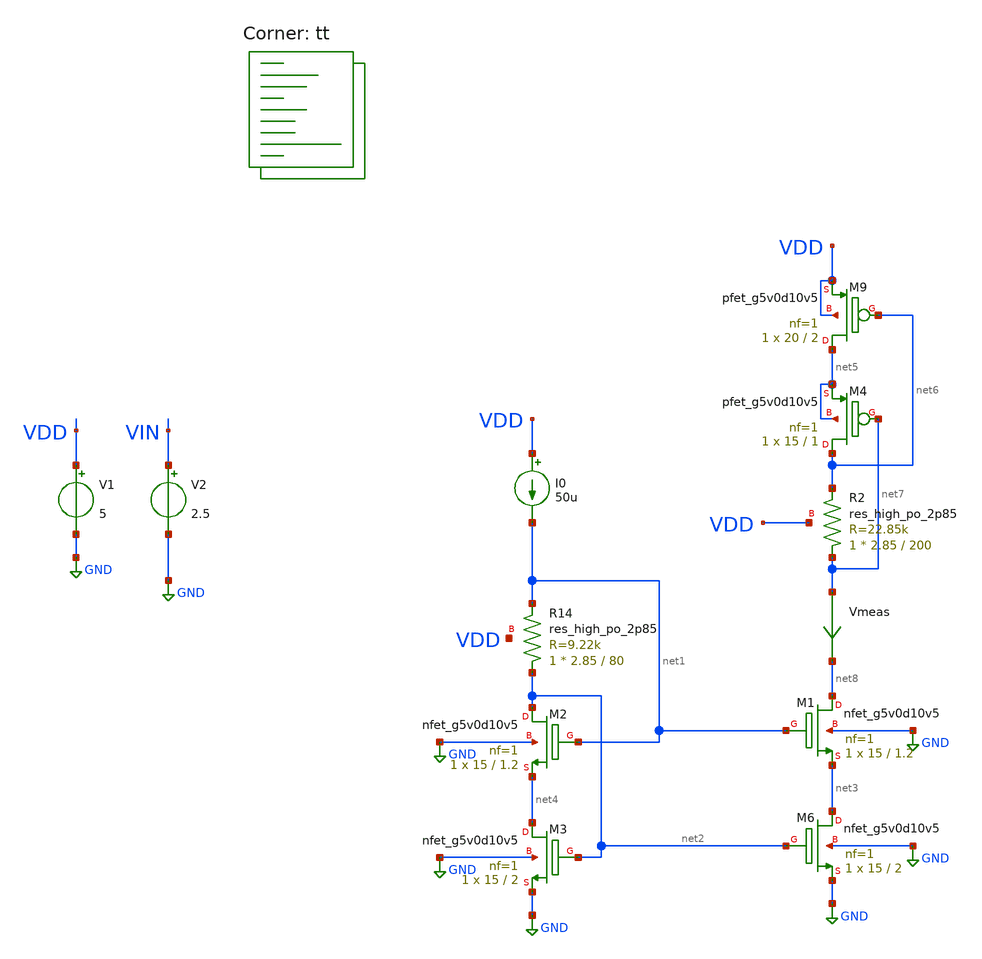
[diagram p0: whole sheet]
** sch_path: old stuff/my_amp_test/third_stage/current_mirror_test.sch
**.subckt current_mirror_test
V1 VDD GND 5
V2 VIN GND 2.5
I0 VDD net1 50u
Vmeas net7 net8 0
.save i(vmeas)
XM2 net2 net1 net4 GND sky130_fd_pr__nfet_g5v0d10v5 L=1.2 W=15 nf=1 ad='int((1 + 1)/2) * 15 / 1 * 0.29'
+ as='int((1 + 2)/2) * 15 / 1 * 0.29' pd='2*int((1 + 1)/2) * (15 / 1 + 0.29)' ps='2*int((1 + 2)/2) * (15 / 1 + 0.29)'
+ nrd='0.29 / 15 ' nrs='0.29 / 15 ' sa=0 sb=0 sd=0 mult=1 m=1
XM3 net4 net2 GND GND sky130_fd_pr__nfet_g5v0d10v5 L=2 W=15 nf=1 ad='int((1 + 1)/2) * 15 / 1 * 0.29'
+ as='int((1 + 2)/2) * 15 / 1 * 0.29' pd='2*int((1 + 1)/2) * (15 / 1 + 0.29)' ps='2*int((1 + 2)/2) * (15 / 1 + 0.29)'
+ nrd='0.29 / 15 ' nrs='0.29 / 15 ' sa=0 sb=0 sd=0 mult=1 m=1
XR14 net2 net1 VDD sky130_fd_pr__res_high_po_2p85 L=80 mult=1 m=1
XM1 net8 net1 net3 GND sky130_fd_pr__nfet_g5v0d10v5 L=1.2 W=15 nf=1 ad='int((1 + 1)/2) * 15 / 1 * 0.29'
+ as='int((1 + 2)/2) * 15 / 1 * 0.29' pd='2*int((1 + 1)/2) * (15 / 1 + 0.29)' ps='2*int((1 + 2)/2) * (15 / 1 + 0.29)'
+ nrd='0.29 / 15 ' nrs='0.29 / 15 ' sa=0 sb=0 sd=0 mult=1 m=1
XM6 net3 net2 GND GND sky130_fd_pr__nfet_g5v0d10v5 L=2 W=15 nf=1 ad='int((1 + 1)/2) * 15 / 1 * 0.29'
+ as='int((1 + 2)/2) * 15 / 1 * 0.29' pd='2*int((1 + 1)/2) * (15 / 1 + 0.29)' ps='2*int((1 + 2)/2) * (15 / 1 + 0.29)'
+ nrd='0.29 / 15 ' nrs='0.29 / 15 ' sa=0 sb=0 sd=0 mult=1 m=1
XR2 net7 net6 VDD sky130_fd_pr__res_high_po_2p85 L=200 mult=1 m=1
XM9 net5 net6 VDD VDD sky130_fd_pr__pfet_g5v0d10v5 L=2 W=20 nf=1 ad='int((1 + 1)/2) * 20 / 1 * 0.29'
+ as='int((1 + 2)/2) * 20 / 1 * 0.29' pd='2*int((1 + 1)/2) * (20 / 1 + 0.29)' ps='2*int((1 + 2)/2) * (20 / 1 + 0.29)'
+ nrd='0.29 / 20 ' nrs='0.29 / 20 ' sa=0 sb=0 sd=0 mult=1 m=1
XM4 net6 net7 net5 net5 sky130_fd_pr__pfet_g5v0d10v5 L=1 W=15 nf=1 ad='int((1 + 1)/2) * 15 / 1 * 0.29'
+ as='int((1 + 2)/2) * 15 / 1 * 0.29' pd='2*int((1 + 1)/2) * (15 / 1 + 0.29)' ps='2*int((1 + 2)/2) * (15 / 1 + 0.29)'
+ nrd='0.29 / 15 ' nrs='0.29 / 15 ' sa=0 sb=0 sd=0 mult=1 m=1
**** begin user architecture code
.lib $::SKYWATER_MODELS/sky130.lib.spice tt

**************************************************************
**************************************************************
**************************************************************
**************************************************************
**************************************************************
*LIBs*********************************************************
**************************************************************
**************************************************************
**************************************************************
**************************************************************
**************************************************************
*.lib $::SKYWATER_MODELS/sky130.lib.spice tt
* chose the corners in the corner file
* tt_mm for mismatch
* ss ff sf fs standart corners
* ll hh lh hl capacitor and resistors corners
* mc for total process variation including corners
**************************************************************
**************************************************************
**************************************************************
**************************************************************
**************************************************************
*Corners/montecarlo options***********************************
**************************************************************
**************************************************************
**************************************************************
**************************************************************
**************************************************************
.TEMP 27
**************************************************************
**************************************************************
**************************************************************
**************************************************************
*SIMULATION and Plots*****************************************
**************************************************************
**************************************************************
**************************************************************
**************************************************************
.control
save all
dc V2 0 5 0.001
*dc simulation
*ploting VIN VOUT and the voltage gain
plot i(Vmeas)
plot 1/deriv(i(Vmeas))
.endc

**** end user architecture code
**.ends
.GLOBAL GND
.end
